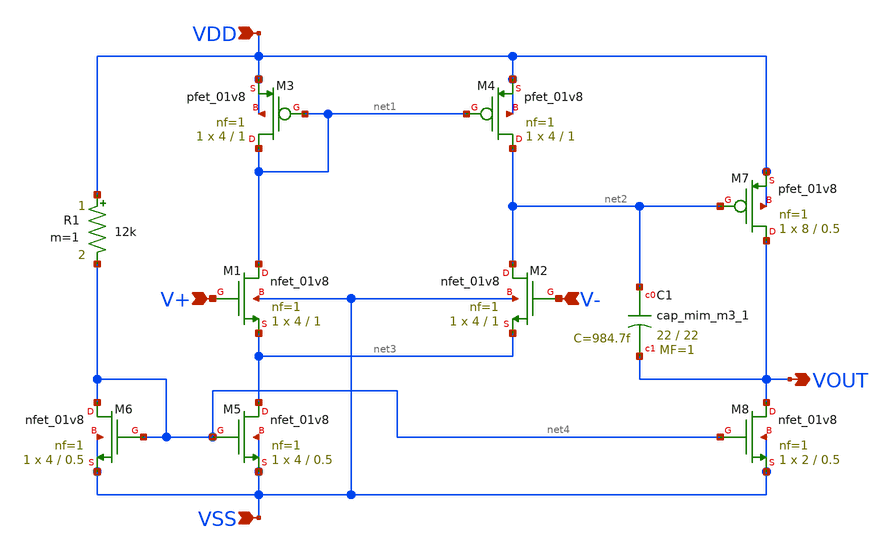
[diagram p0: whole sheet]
** sch_path: analog/schematics/bootcamp_opamp.sch
**.subckt bootcamp_opamp V+ V- VOUT VDD VSS
*.ipin V+
*.ipin V-
*.opin VOUT
*.ipin VDD
*.ipin VSS
XM1 net1 V+ net3 VSS sky130_fd_pr__nfet_01v8 L=1 W=4 nf=1 ad='int((nf+1)/2) * W/nf * 0.29' as='int((nf+2)/2) * W/nf * 0.29'
+ pd='2*int((nf+1)/2) * (W/nf + 0.29)' ps='2*int((nf+2)/2) * (W/nf + 0.29)' nrd='0.29 / W' nrs='0.29 / W'
+ sa=0 sb=0 sd=0 mult=1 m=1
XM2 net2 V- net3 VSS sky130_fd_pr__nfet_01v8 L=1 W=4 nf=1 ad='int((nf+1)/2) * W/nf * 0.29' as='int((nf+2)/2) * W/nf * 0.29'
+ pd='2*int((nf+1)/2) * (W/nf + 0.29)' ps='2*int((nf+2)/2) * (W/nf + 0.29)' nrd='0.29 / W' nrs='0.29 / W'
+ sa=0 sb=0 sd=0 mult=1 m=1
XM3 net1 net1 VDD VDD sky130_fd_pr__pfet_01v8 L=1 W=4 nf=1 ad='int((nf+1)/2) * W/nf * 0.29' as='int((nf+2)/2) * W/nf * 0.29'
+ pd='2*int((nf+1)/2) * (W/nf + 0.29)' ps='2*int((nf+2)/2) * (W/nf + 0.29)' nrd='0.29 / W' nrs='0.29 / W'
+ sa=0 sb=0 sd=0 mult=1 m=1
XM4 net2 net1 VDD VDD sky130_fd_pr__pfet_01v8 L=1 W=4 nf=1 ad='int((nf+1)/2) * W/nf * 0.29' as='int((nf+2)/2) * W/nf * 0.29'
+ pd='2*int((nf+1)/2) * (W/nf + 0.29)' ps='2*int((nf+2)/2) * (W/nf + 0.29)' nrd='0.29 / W' nrs='0.29 / W'
+ sa=0 sb=0 sd=0 mult=1 m=1
XM5 net3 net4 VSS VSS sky130_fd_pr__nfet_01v8 L=0.5 W=4 nf=1 ad='int((nf+1)/2) * W/nf * 0.29' as='int((nf+2)/2) * W/nf * 0.29'
+ pd='2*int((nf+1)/2) * (W/nf + 0.29)' ps='2*int((nf+2)/2) * (W/nf + 0.29)' nrd='0.29 / W' nrs='0.29 / W'
+ sa=0 sb=0 sd=0 mult=1 m=1
XM6 net4 net4 VSS VSS sky130_fd_pr__nfet_01v8 L=0.5 W=4 nf=1 ad='int((nf+1)/2) * W/nf * 0.29' as='int((nf+2)/2) * W/nf * 0.29'
+ pd='2*int((nf+1)/2) * (W/nf + 0.29)' ps='2*int((nf+2)/2) * (W/nf + 0.29)' nrd='0.29 / W' nrs='0.29 / W'
+ sa=0 sb=0 sd=0 mult=1 m=1
XM8 VOUT net4 VSS VSS sky130_fd_pr__nfet_01v8 L=0.5 W=2 nf=1 ad='int((nf+1)/2) * W/nf * 0.29' as='int((nf+2)/2) * W/nf * 0.29'
+ pd='2*int((nf+1)/2) * (W/nf + 0.29)' ps='2*int((nf+2)/2) * (W/nf + 0.29)' nrd='0.29 / W' nrs='0.29 / W'
+ sa=0 sb=0 sd=0 mult=1 m=1
XC1 net2 VOUT sky130_fd_pr__cap_mim_m3_1 W=22 L=22 MF=1 m=1
R1 VDD net4 12k m=1
XM7 VOUT net2 VDD VDD sky130_fd_pr__pfet_01v8 L=0.5 W=8 nf=1 ad='int((nf+1)/2) * W/nf * 0.29' as='int((nf+2)/2) * W/nf * 0.29'
+ pd='2*int((nf+1)/2) * (W/nf + 0.29)' ps='2*int((nf+2)/2) * (W/nf + 0.29)' nrd='0.29 / W' nrs='0.29 / W'
+ sa=0 sb=0 sd=0 mult=1 m=1
**.ends
.end
